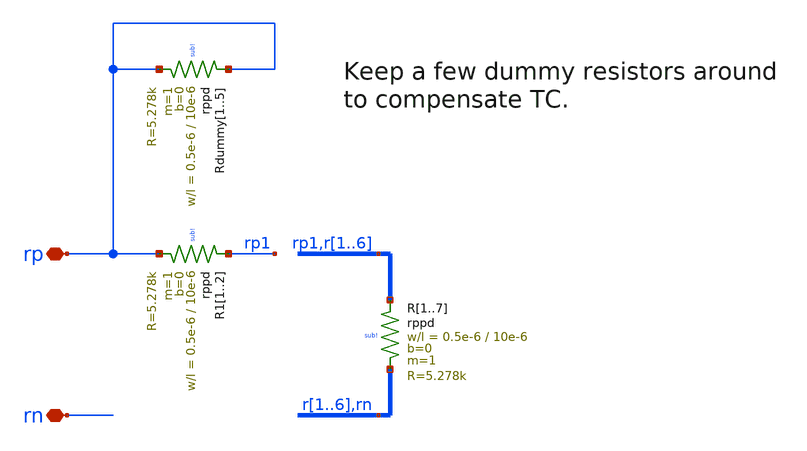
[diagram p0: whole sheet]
** sch_path: xschem/bandgap_simple_res-37k5.sch
* (c) 2025 H. Pretl, Apache-2.0 license
**.subckt bandgap_simple_res-37k5 rp rn
*.iopin rp
*.iopin rn
XR1 rp1 r1 sub! rppd w=0.5e-6 l=10e-6 m=1 b=0 mm_ok=1
XR2 r1 r2 sub! rppd w=0.5e-6 l=10e-6 m=1 b=0 mm_ok=1
XR3 r2 r3 sub! rppd w=0.5e-6 l=10e-6 m=1 b=0 mm_ok=1
XR4 r3 r4 sub! rppd w=0.5e-6 l=10e-6 m=1 b=0 mm_ok=1
XR5 r4 r5 sub! rppd w=0.5e-6 l=10e-6 m=1 b=0 mm_ok=1
XR6 r5 r6 sub! rppd w=0.5e-6 l=10e-6 m=1 b=0 mm_ok=1
XR7 r6 rn sub! rppd w=0.5e-6 l=10e-6 m=1 b=0 mm_ok=1
XR11 rp1 rp sub! rppd w=0.5e-6 l=10e-6 m=1 b=0 mm_ok=1
XR12 rp1 rp sub! rppd w=0.5e-6 l=10e-6 m=1 b=0 mm_ok=1
XRdummy1 rp rp sub! rppd w=0.5e-6 l=10e-6 m=1 b=0 mm_ok=1
XRdummy2 rp rp sub! rppd w=0.5e-6 l=10e-6 m=1 b=0 mm_ok=1
XRdummy3 rp rp sub! rppd w=0.5e-6 l=10e-6 m=1 b=0 mm_ok=1
XRdummy4 rp rp sub! rppd w=0.5e-6 l=10e-6 m=1 b=0 mm_ok=1
XRdummy5 rp rp sub! rppd w=0.5e-6 l=10e-6 m=1 b=0 mm_ok=1
**.ends
.end
